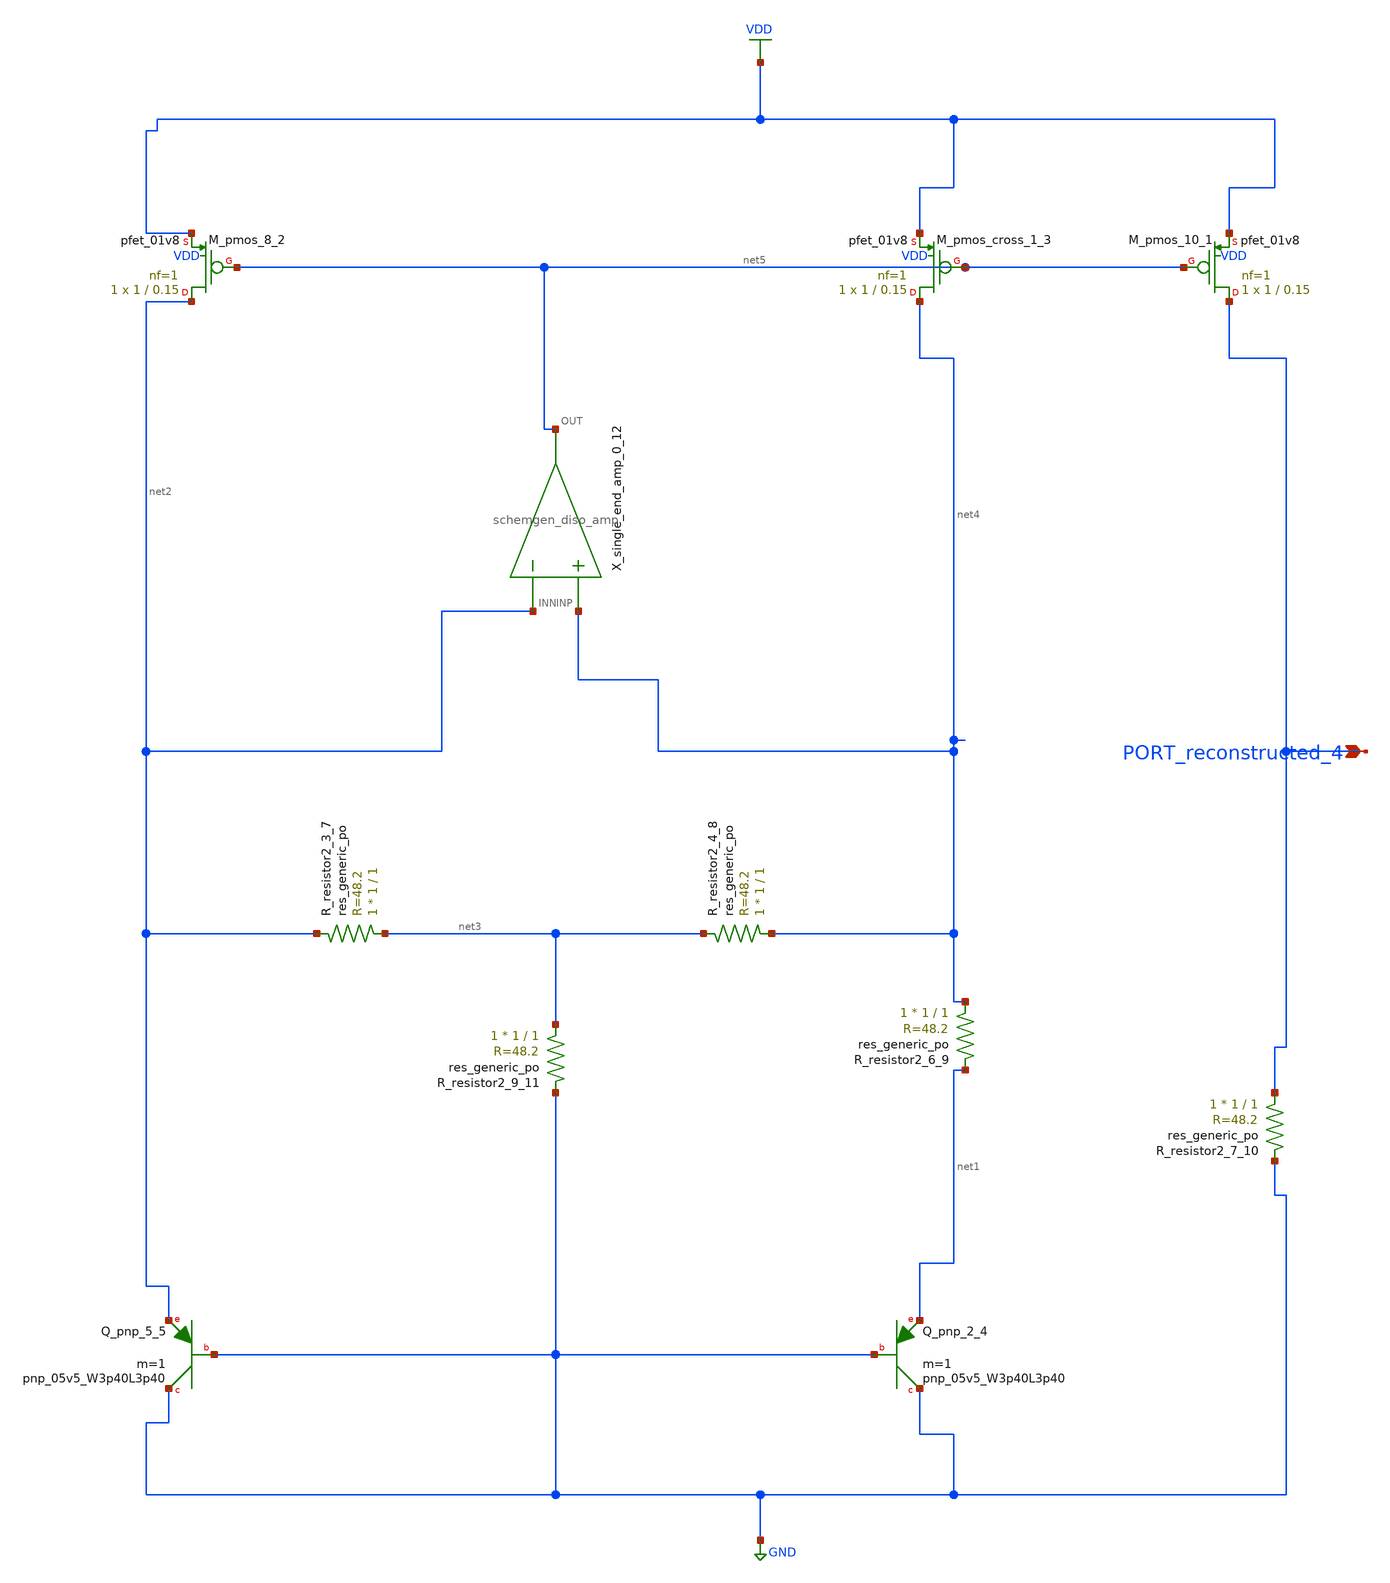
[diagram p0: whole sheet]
** sch_path: schematics/Image2Net/016.sch
**.subckt 016 PORT_reconstructed_4
*.ipin PORT_reconstructed_4
XM_pmos_10_1 PORT_reconstructed_4 net5 VDD VDD sky130_fd_pr__pfet_01v8 L=0.15 W=1 nf=1 ad='int((1 + 1)/2) * 1 / 1 * 0.29'
+ as='int((1 + 2)/2) * 1 / 1 * 0.29' pd='2*int((1 + 1)/2) * (1 / 1 + 0.29)' ps='2*int((1 + 2)/2) * (1 / 1 + 0.29)'
+ nrd='0.29 / 1 ' nrs='0.29 / 1 ' sa=0 sb=0 sd=0 mult=1 m=1
XM_pmos_8_2 net2 net5 VDD VDD sky130_fd_pr__pfet_01v8 L=0.15 W=1 nf=1 ad='int((1 + 1)/2) * 1 / 1 * 0.29'
+ as='int((1 + 2)/2) * 1 / 1 * 0.29' pd='2*int((1 + 1)/2) * (1 / 1 + 0.29)' ps='2*int((1 + 2)/2) * (1 / 1 + 0.29)'
+ nrd='0.29 / 1 ' nrs='0.29 / 1 ' sa=0 sb=0 sd=0 mult=1 m=1
XM_pmos_cross_1_3 net4 net5 VDD VDD sky130_fd_pr__pfet_01v8 L=0.15 W=1 nf=1 ad='int((1 + 1)/2) * 1 / 1 * 0.29'
+ as='int((1 + 2)/2) * 1 / 1 * 0.29' pd='2*int((1 + 1)/2) * (1 / 1 + 0.29)' ps='2*int((1 + 2)/2) * (1 / 1 + 0.29)'
+ nrd='0.29 / 1 ' nrs='0.29 / 1 ' sa=0 sb=0 sd=0 mult=1 m=1
XQ_pnp_2_4 GND GND net1 sky130_fd_pr__pnp_05v5_W3p40L3p40 m=1
XQ_pnp_5_5 GND GND net2 sky130_fd_pr__pnp_05v5_W3p40L3p40 m=1
XR_resistor2_3_7 net3 net2 sky130_fd_pr__res_generic_po W=1 L=1 m=1
XR_resistor2_4_8 net4 net3 sky130_fd_pr__res_generic_po W=1 L=1 m=1
XR_resistor2_6_9 net4 net1 sky130_fd_pr__res_generic_po W=1 L=1 m=1
XR_resistor2_7_10 PORT_reconstructed_4 GND sky130_fd_pr__res_generic_po W=1 L=1 m=1
XR_resistor2_9_11 net3 GND sky130_fd_pr__res_generic_po W=1 L=1 m=1
X_single_end_amp_0_12 net4 net2 net5 schemgen_diso_amp
**.ends

* expanding   symbol:  schemgen_diso_amp.sym # of pins=3
** sym_path: symbols/schemgen_diso_amp.sym
.subckt schemgen_diso_amp INP INN OUT
* SchemGen ideal op-amp: Vout = 1e5 * (V(INP) - V(INN))
E1 OUT 0 INP INN 1e5
.ends schemgen_diso_amp
.GLOBAL GND
.GLOBAL VDD
.end
